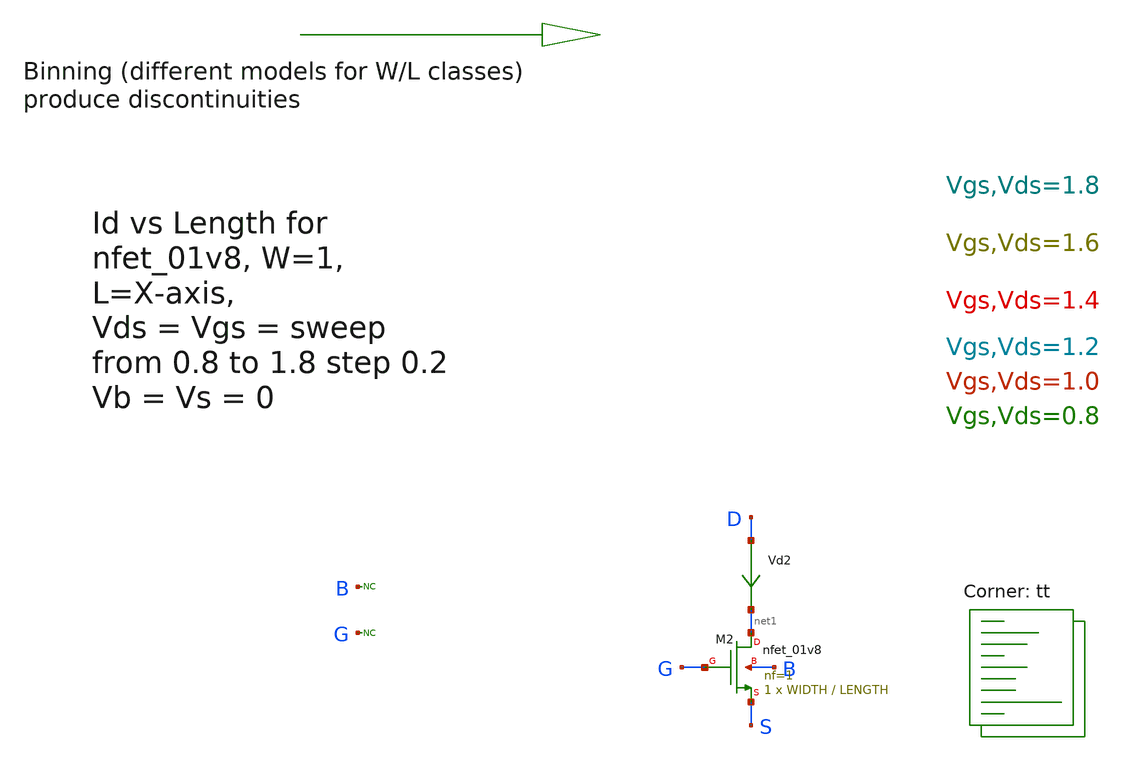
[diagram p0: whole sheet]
** sch_path: sky130A/xschem_libs/sky130_tests/test_mos_binning/schematic/test_mos_binning.sch
* Copyright 2021 Stefan Frederik Schippers
* Licensed under the Apache License, Version 2.0 (the "License");
* you may not use this file except in compliance with the License.
* You may obtain a copy of the License at
* https://www.apache.org/licenses/LICENSE-2.0
* Unless required by applicable law or agreed to in writing, software
* distributed under the License is distributed on an "AS IS" BASIS,
* WITHOUT WARRANTIES OR CONDITIONS OF ANY KIND, either express or implied.
* See the License for the specific language governing permissions and
* limitations under the License.
**.subckt test_mos_binning
Vd2 D net1 0
.save i(vd2)
XM2 net1 G S B sky130_fd_pr__nfet_01v8 L=LENGTH W=WIDTH nf=1 ad='int((1 + 1)/2) * WIDTH / 1 * 0.29' as='int((1 + 2)/2) * WIDTH / 1 * 0.29'
+ pd='2*int((1 + 1)/2) * (WIDTH / 1 + 0.29)' ps='2*int((1 + 2)/2) * (WIDTH / 1 + 0.29)' nrd='0.29 / WIDTH '
+ nrs='0.29 / WIDTH ' sa=0 sb=0 sd=0 mult=1 m=1
* noconn B
* noconn G
**** begin user architecture code


* this option enables mos model bin
* selection based on W/NF instead of W
.option wnflag = 1
.option savecurrents
.param VGATE = 1
.param VDRAIN = 1
.param WIDTH = 1
.param LENGTH=0.15
vd d 0 {VGATE}
vg g 0 {VGATE}
vs s 0 0
vb b 0 0
.control
  save i(vd2)
  ** here we are in the const plot, so declare all vectors.
  let npoints = 100
  let startl = 0.15
  let endl = 1
  let stepl = (endl - startl) / npoints
  let startv = 0.8
  let endv = 1.8
  let stepv = 0.2
  let v = startv
  let i = 0
  let j = startl
  set curplot = new
  set myplot = $curplot
  let curr = vector(npoints + 1)
  let len = vector(npoints + 1)
  while v < endv + stepv / 2
    let i = 0
    let j = startl
    while j <= endl + stepl / 2
      alterparam LENGTH = $&j
      alterparam VGATE = $&v
      reset
      op
      set idx = $&i
      let {$myplot}.curr[i] = i(vd2)
      let {$myplot}.len[i] = j
      let j = j + stepl
      let i = i + 1
    end
    setplot $myplot
    setscale len
    deftype v length L
    settype length len
    settype current curr
    setcs curplottitle = "MOS current vs length sweep"
    setcs curplotname = "DC transfer characteristic"
    write test_mos_binning.raw
    set appendwrite
    let v = v + stepv
  end
.endc


.lib $::SKYWATER_MODELS/sky130.lib.spice tt
**** end user architecture code
**.ends
.end
